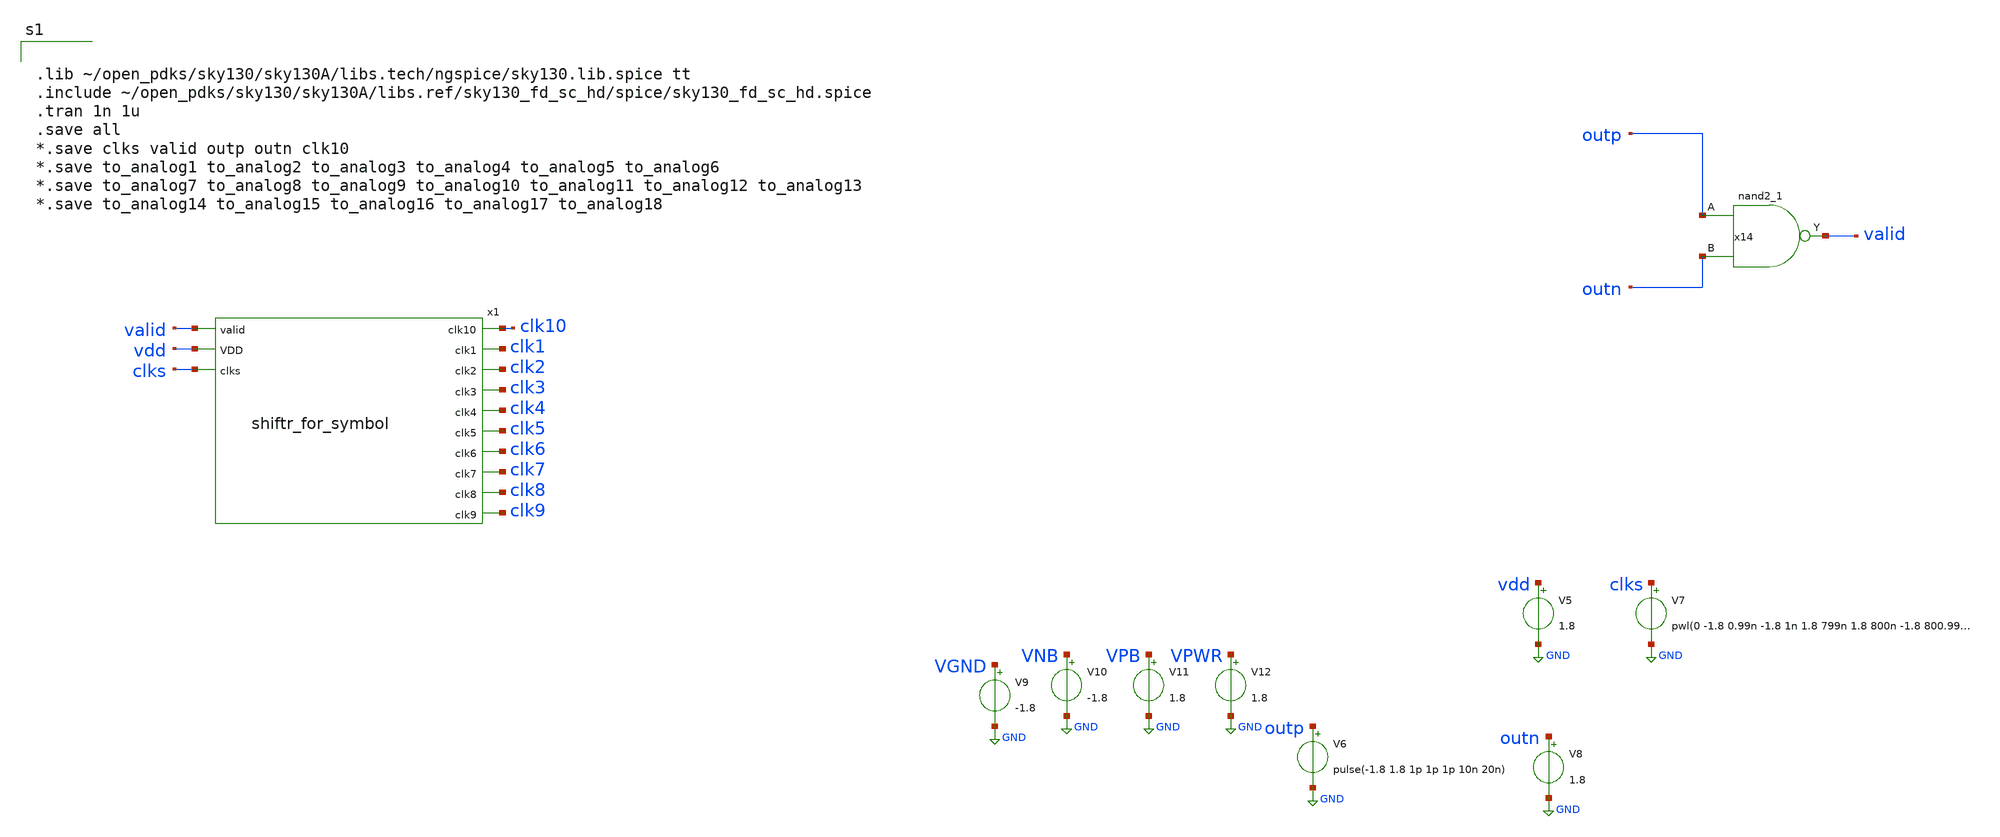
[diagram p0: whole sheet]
** sch_path: d_logic.sch
**.subckt d_logic
x1 valid clk10 clk1 clk2 clk3 clk4 clk5 clk6 clk7 clk8 clk9 vdd clks shiftr_for_symbol
x14 outp outn VGND VNB VPB VPWR valid sky130_fd_sc_hd__nand2_1
V7 clks GND pwl(0 -1.8 0.99n -1.8 1n 1.8 799n 1.8 800n -1.8 800.99n -1.8 801n 1.8)
V5 vdd GND 1.8
V6 outp GND pulse(-1.8 1.8 1p 1p 1p 10n 20n)
V8 outn GND 1.8
V9 VGND GND -1.8
V10 VNB GND -1.8
V11 VPB GND 1.8
V12 VPWR GND 1.8
**** begin user architecture code


.lib ~/open_pdks/sky130/sky130A/libs.tech/ngspice/sky130.lib.spice tt
.include ~/open_pdks/sky130/sky130A/libs.ref/sky130_fd_sc_hd/spice/sky130_fd_sc_hd.spice
.tran 1n 1u
.save all
*.save clks valid outp outn clk10
*.save to_analog1 to_analog2 to_analog3 to_analog4 to_analog5 to_analog6
*.save to_analog7 to_analog8 to_analog9 to_analog10 to_analog11 to_analog12 to_analog13
*.save to_analog14 to_analog15 to_analog16 to_analog17 to_analog18

**** end user architecture code
**.ends

* expanding   symbol:  /home/cegrahul/Desktop/fyp/shiftr_for_symbol.sym # of pins=13
** sym_path: shiftr_for_symbol.sym
** sch_path: shiftr_for_symbol.sch
.subckt shiftr_for_symbol valid clk10 clk1 clk2 clk3 clk4 clk5 clk6 clk7 clk8 clk9 VDD clks
*.ipin valid
*.ipin VDD
*.ipin clks
*.opin clk1
*.opin clk2
*.opin clk3
*.opin clk4
*.opin clk5
*.opin clk6
*.opin clk7
*.opin clk8
*.opin clk9
*.opin clk10
x1 valid VDD clks VGND VNB VPB VPWR clk1 net1 sky130_fd_sc_hd__dfrbp_2
x2 valid clk1 clks VGND VNB VPB VPWR clk2 net2 sky130_fd_sc_hd__dfrbp_2
x3 valid clk2 clks VGND VNB VPB VPWR clk3 net3 sky130_fd_sc_hd__dfrbp_2
x4 valid clk3 clks VGND VNB VPB VPWR clk4 net4 sky130_fd_sc_hd__dfrbp_2
x5 valid clk4 clks VGND VNB VPB VPWR clk5 net5 sky130_fd_sc_hd__dfrbp_2
x6 valid clk5 clks VGND VNB VPB VPWR clk6 net6 sky130_fd_sc_hd__dfrbp_2
x7 valid clk6 clks VGND VNB VPB VPWR clk7 net7 sky130_fd_sc_hd__dfrbp_2
x8 valid clk7 clks VGND VNB VPB VPWR clk8 net8 sky130_fd_sc_hd__dfrbp_2
x9 valid clk8 clks VGND VNB VPB VPWR clk9 net9 sky130_fd_sc_hd__dfrbp_2
x10 valid clk9 clks VGND VNB VPB VPWR clk10 net10 sky130_fd_sc_hd__dfrbp_2
.ends

.GLOBAL GND
.end
